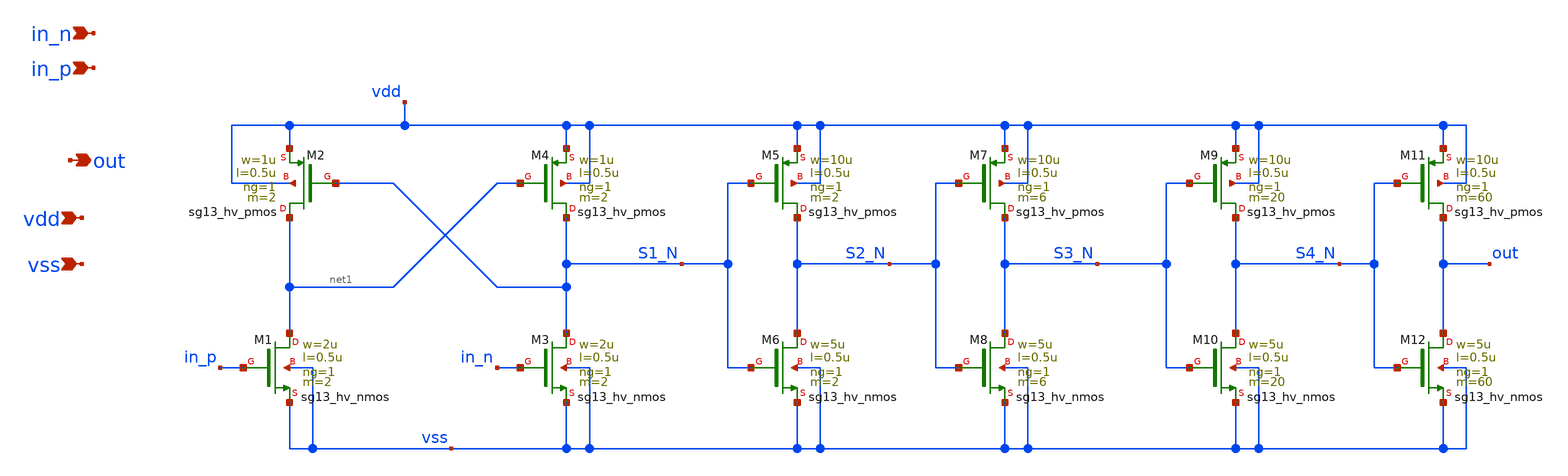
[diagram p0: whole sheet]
** sch_path: xschem/gate_drive_large.sch
**.subckt gate_drive_large in_n in_p vdd vss out
*.ipin in_n
*.ipin in_p
*.ipin vdd
*.ipin vss
*.opin out
XM1 net1 in_p vss vss sg13_hv_nmos w=2u l=0.5u ng=1 m=2 mm_ok=1
XM2 net1 S1_N vdd vdd sg13_hv_pmos w=1u l=0.5u ng=1 m=2 mm_ok=1
XM3 S1_N in_n vss vss sg13_hv_nmos w=2u l=0.5u ng=1 m=2 mm_ok=1
XM4 S1_N net1 vdd vdd sg13_hv_pmos w=1u l=0.5u ng=1 m=2 mm_ok=1
XM5 S2_N S1_N vdd vdd sg13_hv_pmos w=10u l=0.5u ng=1 m=2 mm_ok=1
XM6 S2_N S1_N vss vss sg13_hv_nmos w=5u l=0.5u ng=1 m=2 mm_ok=1
XM7 S3_N S2_N vdd vdd sg13_hv_pmos w=10u l=0.5u ng=1 m=6 mm_ok=1
XM8 S3_N S2_N vss vss sg13_hv_nmos w=5u l=0.5u ng=1 m=6 mm_ok=1
XM9 S4_N S3_N vdd vdd sg13_hv_pmos w=10u l=0.5u ng=1 m=20 mm_ok=1
XM10 S4_N S3_N vss vss sg13_hv_nmos w=5u l=0.5u ng=1 m=20 mm_ok=1
XM11 out S4_N vdd vdd sg13_hv_pmos w=10u l=0.5u ng=1 m=60 mm_ok=1
XM12 out S4_N vss vss sg13_hv_nmos w=5u l=0.5u ng=1 m=60 mm_ok=1
**.ends
.end
